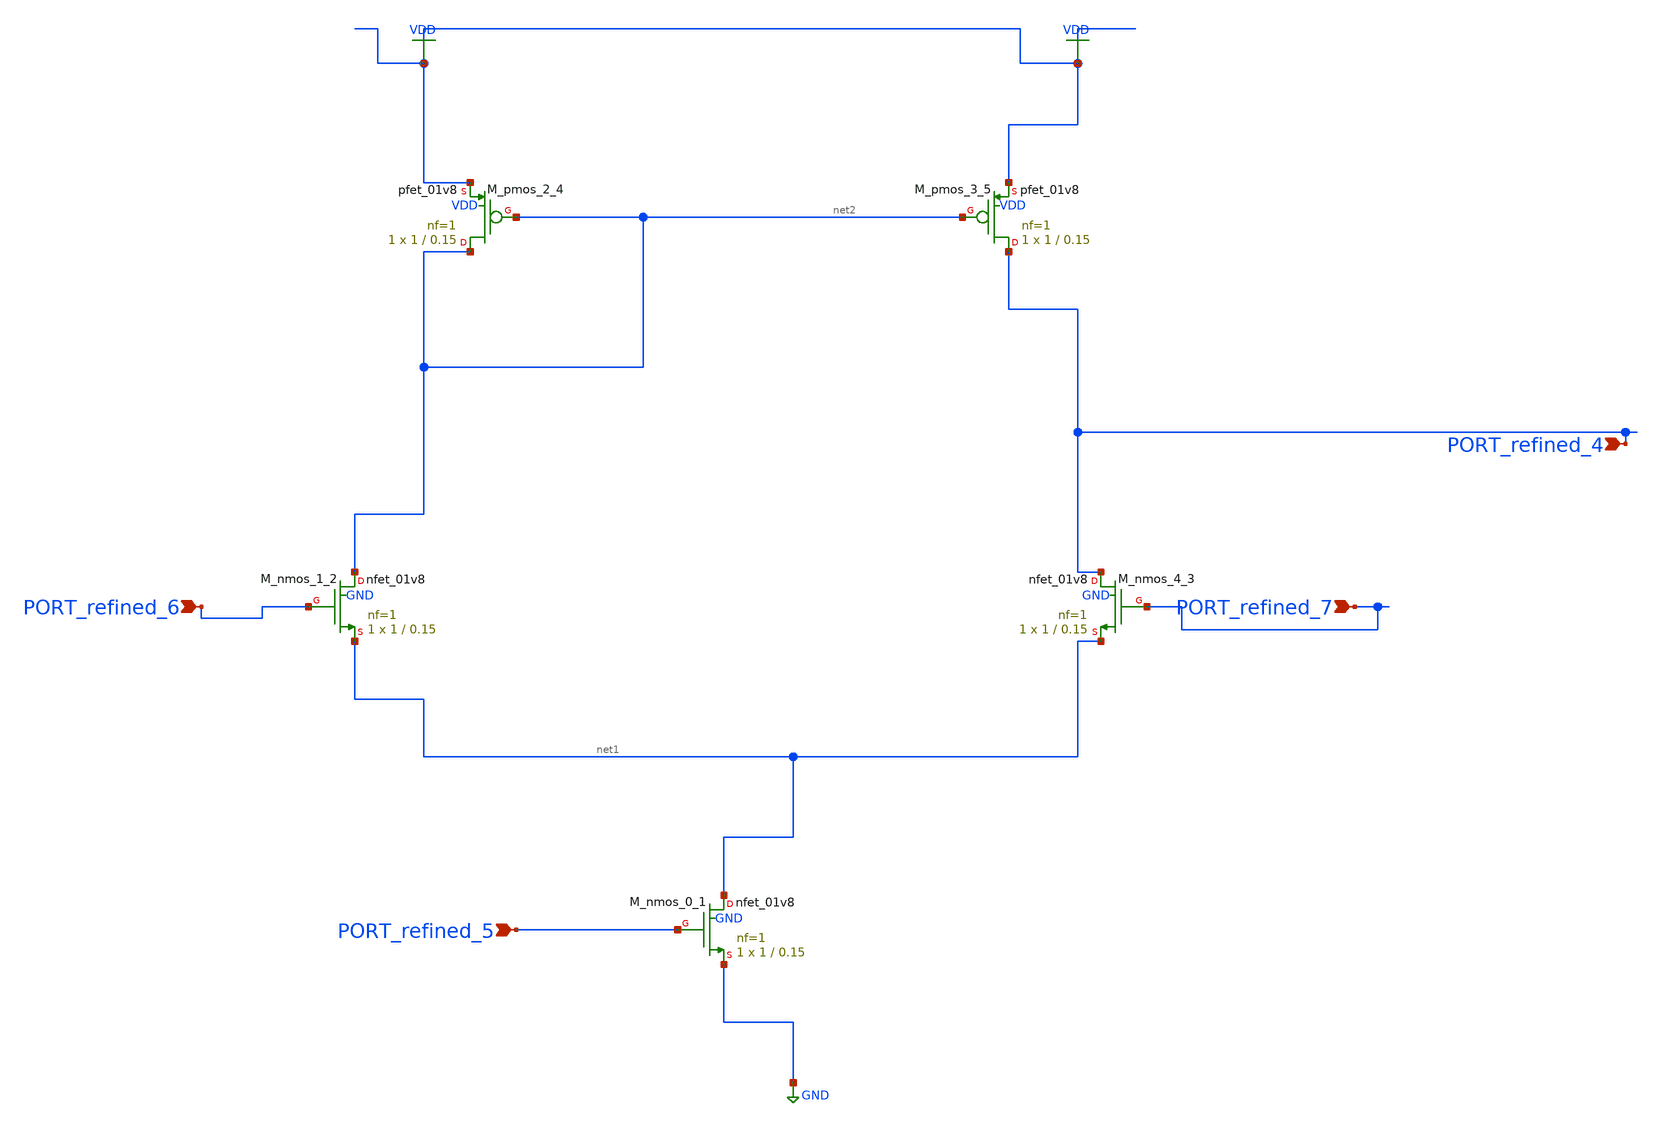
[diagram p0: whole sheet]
** sch_path: schematics/AMSNet/350.sch
**.subckt 350 PORT_refined_7 PORT_refined_5 PORT_refined_6 PORT_refined_4
*.ipin PORT_refined_7
*.ipin PORT_refined_5
*.ipin PORT_refined_6
*.ipin PORT_refined_4
XM_nmos_0_1 net1 PORT_refined_5 GND GND sky130_fd_pr__nfet_01v8 L=0.15 W=1 nf=1 ad='int((1 + 1)/2) * 1 / 1 * 0.29'
+ as='int((1 + 2)/2) * 1 / 1 * 0.29' pd='2*int((1 + 1)/2) * (1 / 1 + 0.29)' ps='2*int((1 + 2)/2) * (1 / 1 + 0.29)'
+ nrd='0.29 / 1 ' nrs='0.29 / 1 ' sa=0 sb=0 sd=0 mult=1 m=1
XM_nmos_1_2 net2 PORT_refined_6 net1 GND sky130_fd_pr__nfet_01v8 L=0.15 W=1 nf=1 ad='int((1 + 1)/2) * 1 / 1 * 0.29'
+ as='int((1 + 2)/2) * 1 / 1 * 0.29' pd='2*int((1 + 1)/2) * (1 / 1 + 0.29)' ps='2*int((1 + 2)/2) * (1 / 1 + 0.29)'
+ nrd='0.29 / 1 ' nrs='0.29 / 1 ' sa=0 sb=0 sd=0 mult=1 m=1
XM_nmos_4_3 PORT_refined_4 PORT_refined_7 net1 GND sky130_fd_pr__nfet_01v8 L=0.15 W=1 nf=1 ad='int((1 + 1)/2) * 1 / 1 * 0.29'
+ as='int((1 + 2)/2) * 1 / 1 * 0.29' pd='2*int((1 + 1)/2) * (1 / 1 + 0.29)' ps='2*int((1 + 2)/2) * (1 / 1 + 0.29)'
+ nrd='0.29 / 1 ' nrs='0.29 / 1 ' sa=0 sb=0 sd=0 mult=1 m=1
XM_pmos_2_4 net2 net2 VDD VDD sky130_fd_pr__pfet_01v8 L=0.15 W=1 nf=1 ad='int((1 + 1)/2) * 1 / 1 * 0.29'
+ as='int((1 + 2)/2) * 1 / 1 * 0.29' pd='2*int((1 + 1)/2) * (1 / 1 + 0.29)' ps='2*int((1 + 2)/2) * (1 / 1 + 0.29)'
+ nrd='0.29 / 1 ' nrs='0.29 / 1 ' sa=0 sb=0 sd=0 mult=1 m=1
XM_pmos_3_5 PORT_refined_4 net2 VDD VDD sky130_fd_pr__pfet_01v8 L=0.15 W=1 nf=1 ad='int((1 + 1)/2) * 1 / 1 * 0.29'
+ as='int((1 + 2)/2) * 1 / 1 * 0.29' pd='2*int((1 + 1)/2) * (1 / 1 + 0.29)' ps='2*int((1 + 2)/2) * (1 / 1 + 0.29)'
+ nrd='0.29 / 1 ' nrs='0.29 / 1 ' sa=0 sb=0 sd=0 mult=1 m=1
**.ends
.GLOBAL GND
.GLOBAL VDD
.end
